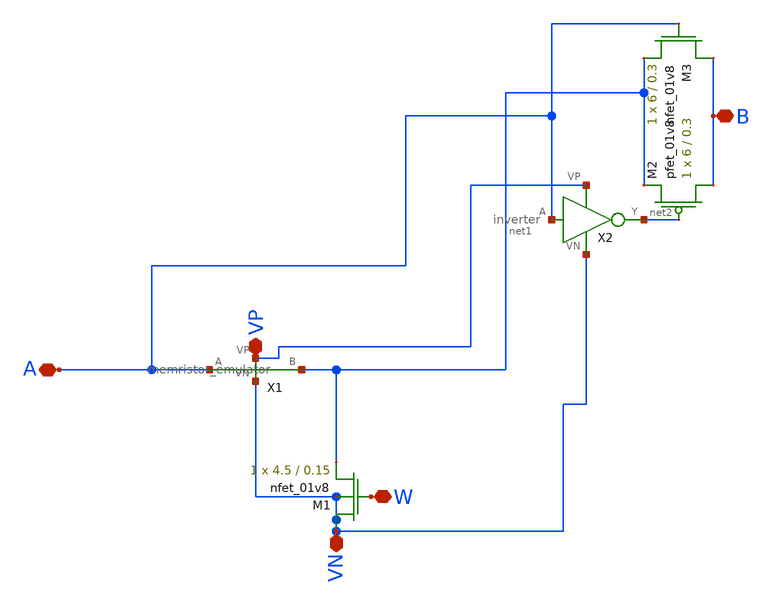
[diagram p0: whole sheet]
** sch_path: schematic/res.sch
**.subckt res A W VP VN B
*.iopin A
*.iopin W
*.iopin VP
*.iopin VN
*.iopin B
XM1 VN W net1 VN sky130_fd_pr__nfet_01v8 L=0.15 W=4.5 nf=1 ad='int((nf+1)/2) * W/nf * 0.29' as='int((nf+2)/2) * W/nf * 0.29'
+ pd='2*int((nf+1)/2) * (W/nf + 0.29)' ps='2*int((nf+2)/2) * (W/nf + 0.29)' nrd='0.29 / W' nrs='0.29 / W'
+ sa=0 sb=0 sd=0 mult=1 m=1
X1 VP VN net1 A memristor_emulator
XM2 B net2 net1 VP sky130_fd_pr__pfet_01v8 L=0.3 W=6 nf=1 ad='int((nf+1)/2) * W/nf * 0.29' as='int((nf+2)/2) * W/nf * 0.29'
+ pd='2*int((nf+1)/2) * (W/nf + 0.29)' ps='2*int((nf+2)/2) * (W/nf + 0.29)' nrd='0.29 / W' nrs='0.29 / W'
+ sa=0 sb=0 sd=0 mult=1 m=1
XM3 B A net1 VN sky130_fd_pr__nfet_01v8 L=0.3 W=6 nf=1 ad='int((nf+1)/2) * W/nf * 0.29' as='int((nf+2)/2) * W/nf * 0.29'
+ pd='2*int((nf+1)/2) * (W/nf + 0.29)' ps='2*int((nf+2)/2) * (W/nf + 0.29)' nrd='0.29 / W' nrs='0.29 / W'
+ sa=0 sb=0 sd=0 mult=1 m=1
X2 A VN VP net2 inverter
**.ends

* expanding   symbol:  /home/madvlsi/neuromorphic_computing_final/schematic/memristor_emulator.sym #
*+ of pins=4
** sym_path: schematic/memristor_emulator.sym
** sch_path: schematic/memristor_emulator.sch
.subckt memristor_emulator VP VN B A
*.ipin A
*.iopin VN
*.iopin VP
*.opin B
XM1 B in_cap A B sky130_fd_pr__pfet_01v8 L=0.3 W=12 nf=1 ad='int((nf+1)/2) * W/nf * 0.29' as='int((nf+2)/2) * W/nf * 0.29'
+ pd='2*int((nf+1)/2) * (W/nf + 0.29)' ps='2*int((nf+2)/2) * (W/nf + 0.29)' nrd='0.29 / W' nrs='0.29 / W'
+ sa=0 sb=0 sd=0 mult=1 m=1
XM2 VP A in_cap VP sky130_fd_pr__pfet_01v8 L=2 W=3 nf=1 ad='int((nf+1)/2) * W/nf * 0.29' as='int((nf+2)/2) * W/nf * 0.29'
+ pd='2*int((nf+1)/2) * (W/nf + 0.29)' ps='2*int((nf+2)/2) * (W/nf + 0.29)' nrd='0.29 / W' nrs='0.29 / W'
+ sa=0 sb=0 sd=0 mult=1 m=1
XM3 VN in_cap VN VN sky130_fd_pr__nfet_01v8 L=20 W=20 nf=1 ad='int((nf+1)/2) * W/nf * 0.29' as='int((nf+2)/2) * W/nf * 0.29'
+ pd='2*int((nf+1)/2) * (W/nf + 0.29)' ps='2*int((nf+2)/2) * (W/nf + 0.29)' nrd='0.29 / W' nrs='0.29 / W'
+ sa=0 sb=0 sd=0 mult=1 m=1
XM4 VN B in_cap VN sky130_fd_pr__nfet_01v8 L=3 W=2 nf=1 ad='int((nf+1)/2) * W/nf * 0.29' as='int((nf+2)/2) * W/nf * 0.29'
+ pd='2*int((nf+1)/2) * (W/nf + 0.29)' ps='2*int((nf+2)/2) * (W/nf + 0.29)' nrd='0.29 / W' nrs='0.29 / W'
+ sa=0 sb=0 sd=0 mult=1 m=1
.ends


* expanding   symbol:  /home/madvlsi/neuromorphic_computing_final/schematic/inverter.sym # of pins=4
** sym_path: schematic/inverter.sym
** sch_path: schematic/inverter.sch
.subckt inverter A VN VP Y
*.ipin A
*.iopin VP
*.iopin VN
*.opin Y
XM1 Y A VN VN sky130_fd_pr__nfet_01v8 L=0.15 W=1 nf=1 ad='int((nf+1)/2) * W/nf * 0.29' as='int((nf+2)/2) * W/nf * 0.29'
+ pd='2*int((nf+1)/2) * (W/nf + 0.29)' ps='2*int((nf+2)/2) * (W/nf + 0.29)' nrd='0.29 / W' nrs='0.29 / W'
+ sa=0 sb=0 sd=0 mult=1 m=1
XM2 Y A VP VP sky130_fd_pr__pfet_01v8 L=0.15 W=1 nf=1 ad='int((nf+1)/2) * W/nf * 0.29' as='int((nf+2)/2) * W/nf * 0.29'
+ pd='2*int((nf+1)/2) * (W/nf + 0.29)' ps='2*int((nf+2)/2) * (W/nf + 0.29)' nrd='0.29 / W' nrs='0.29 / W'
+ sa=0 sb=0 sd=0 mult=1 m=1
.ends

.end
